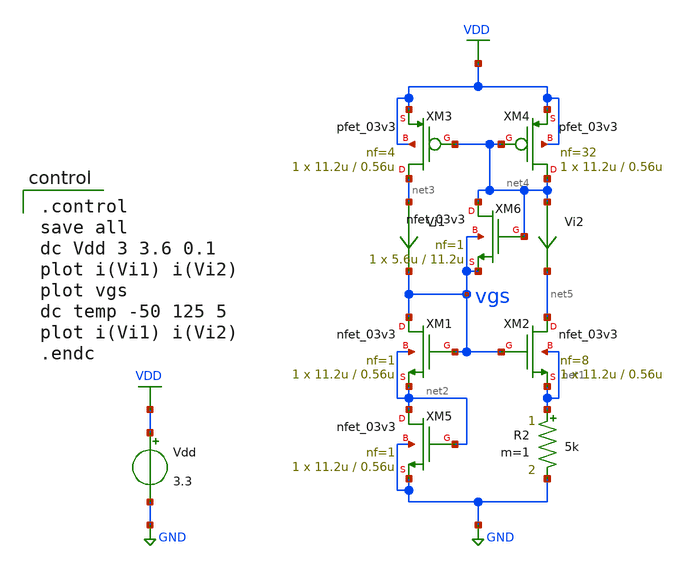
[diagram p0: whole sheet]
** sch_path: current-source/cs-startup-widlar.sch
**.subckt cs-startup-widlar
Vdd VDD GND 3.3
XM1 vgs vgs net2 net2 nfet_03v3 L=0.56u W=11.2u nf=1 ad='int((nf+1)/2) * W/nf * 0.18u' as='int((nf+2)/2) * W/nf * 0.18u'
+ pd='2*int((nf+1)/2) * (W/nf + 0.18u)' ps='2*int((nf+2)/2) * (W/nf + 0.18u)' nrd='0.18u / W' nrs='0.18u / W'
+ sa=0 sb=0 sd=0 m=1
XM2 net5 vgs net1 net1 nfet_03v3 L=0.56u W=11.2u nf=8 ad='int((nf+1)/2) * W/nf * 0.18u' as='int((nf+2)/2) * W/nf * 0.18u'
+ pd='2*int((nf+1)/2) * (W/nf + 0.18u)' ps='2*int((nf+2)/2) * (W/nf + 0.18u)' nrd='0.18u / W' nrs='0.18u / W'
+ sa=0 sb=0 sd=0 m=1
Vi1 net3 vgs 0
.save i(vi1)
Vi2 net4 net5 0
.save i(vi2)
R2 net1 GND 5k m=1
XM3 net3 net4 VDD VDD pfet_03v3 L=0.56u W=11.2u nf=4 ad='int((nf+1)/2) * W/nf * 0.18u' as='int((nf+2)/2) * W/nf * 0.18u'
+ pd='2*int((nf+1)/2) * (W/nf + 0.18u)' ps='2*int((nf+2)/2) * (W/nf + 0.18u)' nrd='0.18u / W' nrs='0.18u / W'
+ sa=0 sb=0 sd=0 m=1
XM4 net4 net4 VDD VDD pfet_03v3 L=0.56u W=11.2u nf=32 ad='int((nf+1)/2) * W/nf * 0.18u' as='int((nf+2)/2) * W/nf * 0.18u'
+ pd='2*int((nf+1)/2) * (W/nf + 0.18u)' ps='2*int((nf+2)/2) * (W/nf + 0.18u)' nrd='0.18u / W' nrs='0.18u / W'
+ sa=0 sb=0 sd=0 m=1
XM5 net2 net2 GND GND nfet_03v3 L=0.56u W=11.2u nf=1 ad='int((nf+1)/2) * W/nf * 0.18u' as='int((nf+2)/2) * W/nf * 0.18u'
+ pd='2*int((nf+1)/2) * (W/nf + 0.18u)' ps='2*int((nf+2)/2) * (W/nf + 0.18u)' nrd='0.18u / W' nrs='0.18u / W'
+ sa=0 sb=0 sd=0 m=1
XM6 net4 net4 vgs vgs nfet_03v3 L=11.2u W=5.6u nf=1 ad='int((nf+1)/2) * W/nf * 0.18u' as='int((nf+2)/2) * W/nf * 0.18u'
+ pd='2*int((nf+1)/2) * (W/nf + 0.18u)' ps='2*int((nf+2)/2) * (W/nf + 0.18u)' nrd='0.18u / W' nrs='0.18u / W'
+ sa=0 sb=0 sd=0 m=1
**** begin user architecture code

.include $::180MCU_MODELS/design.ngspice
.lib $::180MCU_MODELS/sm141064.ngspice typical
.lib $::180MCU_MODELS/sm141064.ngspice res_typical
.lib $::180MCU_MODELS/sm141064.ngspice moscap_typical
.lib $::180MCU_MODELS/sm141064.ngspice bjt_typical
* .lib $::180MCU_MODELS/sm141064.ngspice res_statistical


.control
save all
dc Vdd 3 3.6 0.1
plot i(Vi1) i(Vi2)
plot vgs
dc temp -50 125 5
plot i(Vi1) i(Vi2)
.endc

**** end user architecture code
**.ends
.GLOBAL GND
.GLOBAL VDD
.end
